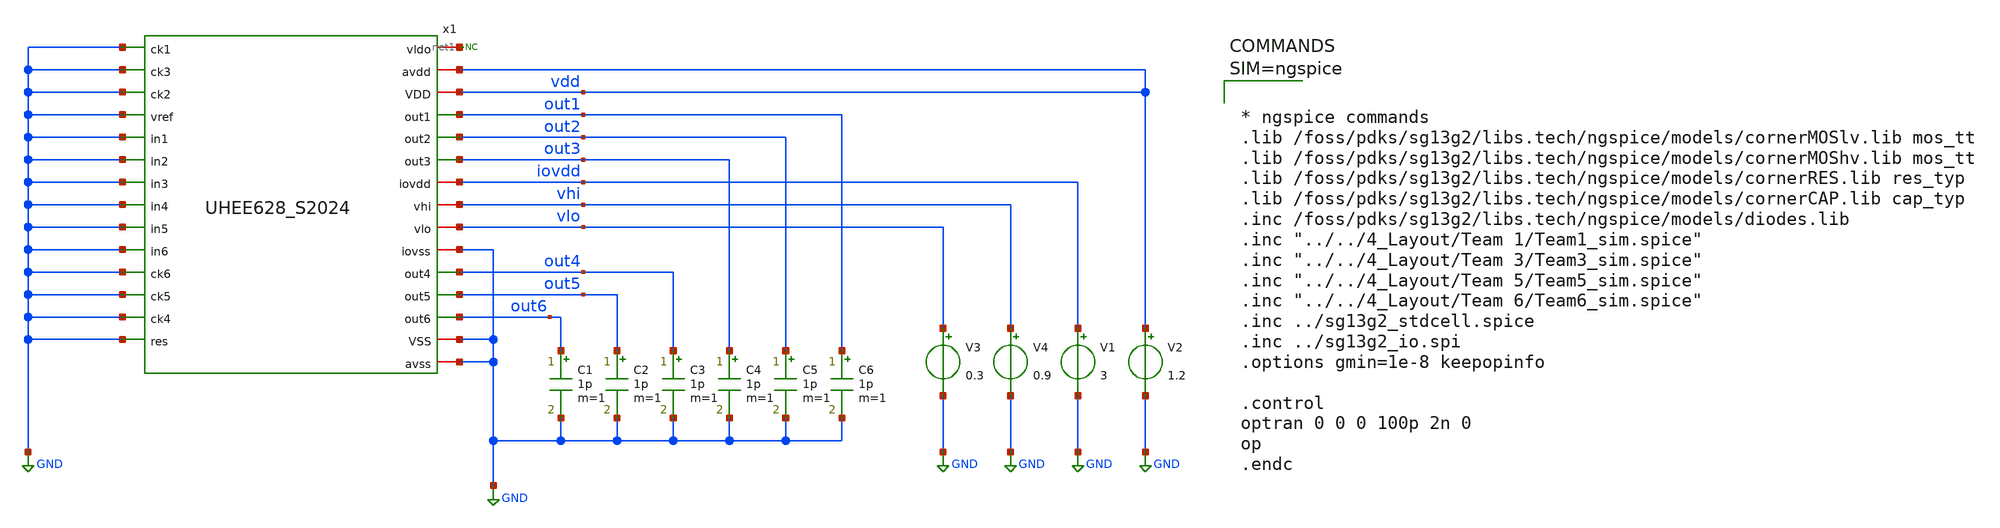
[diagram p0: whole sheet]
** sch_path: 5_Design/3_Real_circuits/tb_UHEE628_S2024.sch
**.subckt tb_UHEE628_S2024
x1 net1 GND GND vdd GND vdd GND out1 GND GND out2 out3 GND iovdd vhi vlo GND out4 GND out5 GND out6
+ GND GND GND GND GND GND GND UHEE628_S2024
V1 iovdd GND 3
V2 vdd GND 1.2
* noconn #net1
V3 vlo GND 0.3
V4 vhi GND 0.9
C1 out6 GND 1p m=1
C2 out5 GND 1p m=1
C3 out4 GND 1p m=1
C4 out3 GND 1p m=1
C5 out2 GND 1p m=1
C6 out1 GND 1p m=1
**** begin user architecture code



* ngspice commands
.lib /foss/pdks/sg13g2/libs.tech/ngspice/models/cornerMOSlv.lib mos_tt
.lib /foss/pdks/sg13g2/libs.tech/ngspice/models/cornerMOShv.lib mos_tt
.lib /foss/pdks/sg13g2/libs.tech/ngspice/models/cornerRES.lib res_typ
.lib /foss/pdks/sg13g2/libs.tech/ngspice/models/cornerCAP.lib cap_typ
.inc /foss/pdks/sg13g2/libs.tech/ngspice/models/diodes.lib
.inc "../../4_Layout/Team 1/Team1_sim.spice"
.inc "../../4_Layout/Team 3/Team3_sim.spice"
.inc "../../4_Layout/Team 5/Team5_sim.spice"
.inc "../../4_Layout/Team 6/Team6_sim.spice"
.inc ../sg13g2_stdcell.spice
.inc ../sg13g2_io.spi
.options gmin=1e-8 keepopinfo

.control
optran 0 0 0 100p 2n 0
op
.endc


**** end user architecture code
**.ends
.GLOBAL GND
.end
